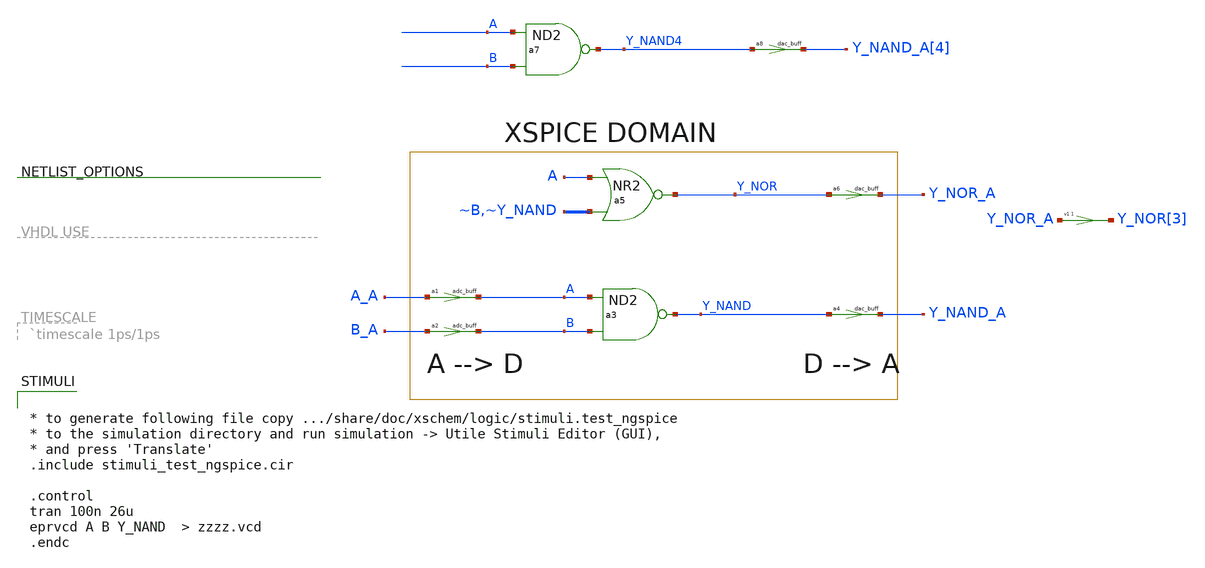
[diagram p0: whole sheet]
** sch_path: xschem_library/logic/test_ngspice.sch
**.subckt test_ngspice
a1 [ A_A ] [ A ] adc_buff
a2 [ B_A ] [ B ] adc_buff
a3 [ A B ] Y_NAND nand
a4 [ Y_NAND ] [ Y_NAND_A ] dac_buff
a6 [ Y_NOR ] [ Y_NOR_A ] dac_buff
a5 [ A ~B ~Y_NAND ] Y_NOR nor
a7 [ A B ] Y_NAND4 nand
a8 [ Y_NAND4 ] [ Y_NAND_A[4] ] dac_buff
v1 Y_NOR[3] Y_NOR_A 0
**** begin user architecture code
.model adc_buff adc_bridge(in_low = 0.3 in_high = 0.7)


.model nand d_nand(rise_delay = 0.5e-9 fall_delay = 0.3e-9  input_load = 5e-15)

.model nor d_nor(rise_delay = 0.7e-9 fall_delay = 0.2e-9  input_load = 5e-15)

.model dac_buff  dac_bridge(out_low = 0 out_high = 1.2 out_undef = 0.6  input_load = 5.0e-15 t_rise
+ = 0.5e-9  t_fall = 0.2e-9)

**** end user architecture code
**.ends
**** begin user architecture code


* to generate following file copy .../share/doc/xschem/logic/stimuli.test_ngspice
* to the simulation directory and run simulation -> Utile Stimuli Editor (GUI),
* and press 'Translate'
.include stimuli_test_ngspice.cir

.control
tran 100n 26u
eprvcd A B Y_NAND  > zzzz.vcd
.endc


**** end user architecture code
.end
